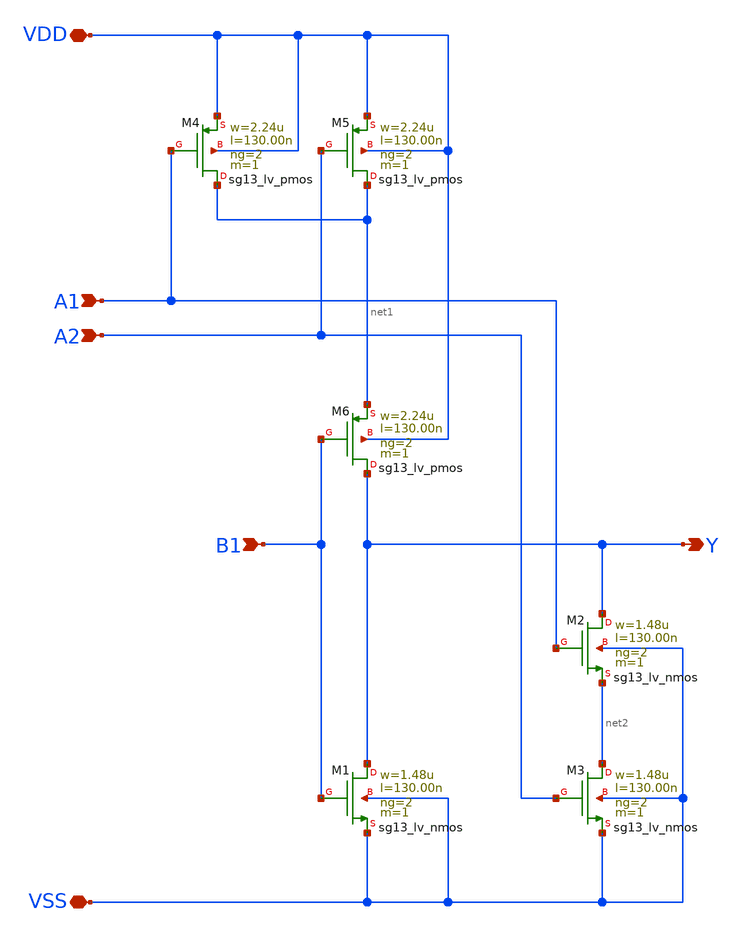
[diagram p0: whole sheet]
** sch_path: ihp-sg13g2/libs.tech/xschem/sg13g2_stdcells/sg13g2_a21oi_2.sch
* Copyright 2023 IHP PDK Authors
* Licensed under the Apache License, Version 2.0 (the "License");
* you may not use this file except in compliance with the License.
* You may obtain a copy of the License at
* https://www.apache.org/licenses/LICENSE-2.0
* Unless required by applicable law or agreed to in writing, software
* distributed under the License is distributed on an "AS IS" BASIS,
* WITHOUT WARRANTIES OR CONDITIONS OF ANY KIND, either express or implied.
* See the License for the specific language governing permissions and
* limitations under the License.
**.subckt sg13g2_a21oi_2 A1 A2 B1 Y VDD VSS
*.ipin A1
*.ipin A2
*.ipin B1
*.opin Y
*.iopin VDD
*.iopin VSS
XM1 Y B1 VSS VSS sg13_lv_nmos w=1.48u l=130.00n ng=2 m=1 mm_ok=1
XM2 Y A1 net2 VSS sg13_lv_nmos w=1.48u l=130.00n ng=2 m=1 mm_ok=1
XM3 net2 A2 VSS VSS sg13_lv_nmos w=1.48u l=130.00n ng=2 m=1 mm_ok=1
XM4 net1 A1 VDD VDD sg13_lv_pmos w=2.24u l=130.00n ng=2 m=1 mm_ok=1
XM5 net1 A2 VDD VDD sg13_lv_pmos w=2.24u l=130.00n ng=2 m=1 mm_ok=1
XM6 Y B1 net1 VDD sg13_lv_pmos w=2.24u l=130.00n ng=2 m=1 mm_ok=1
**.ends
.end
